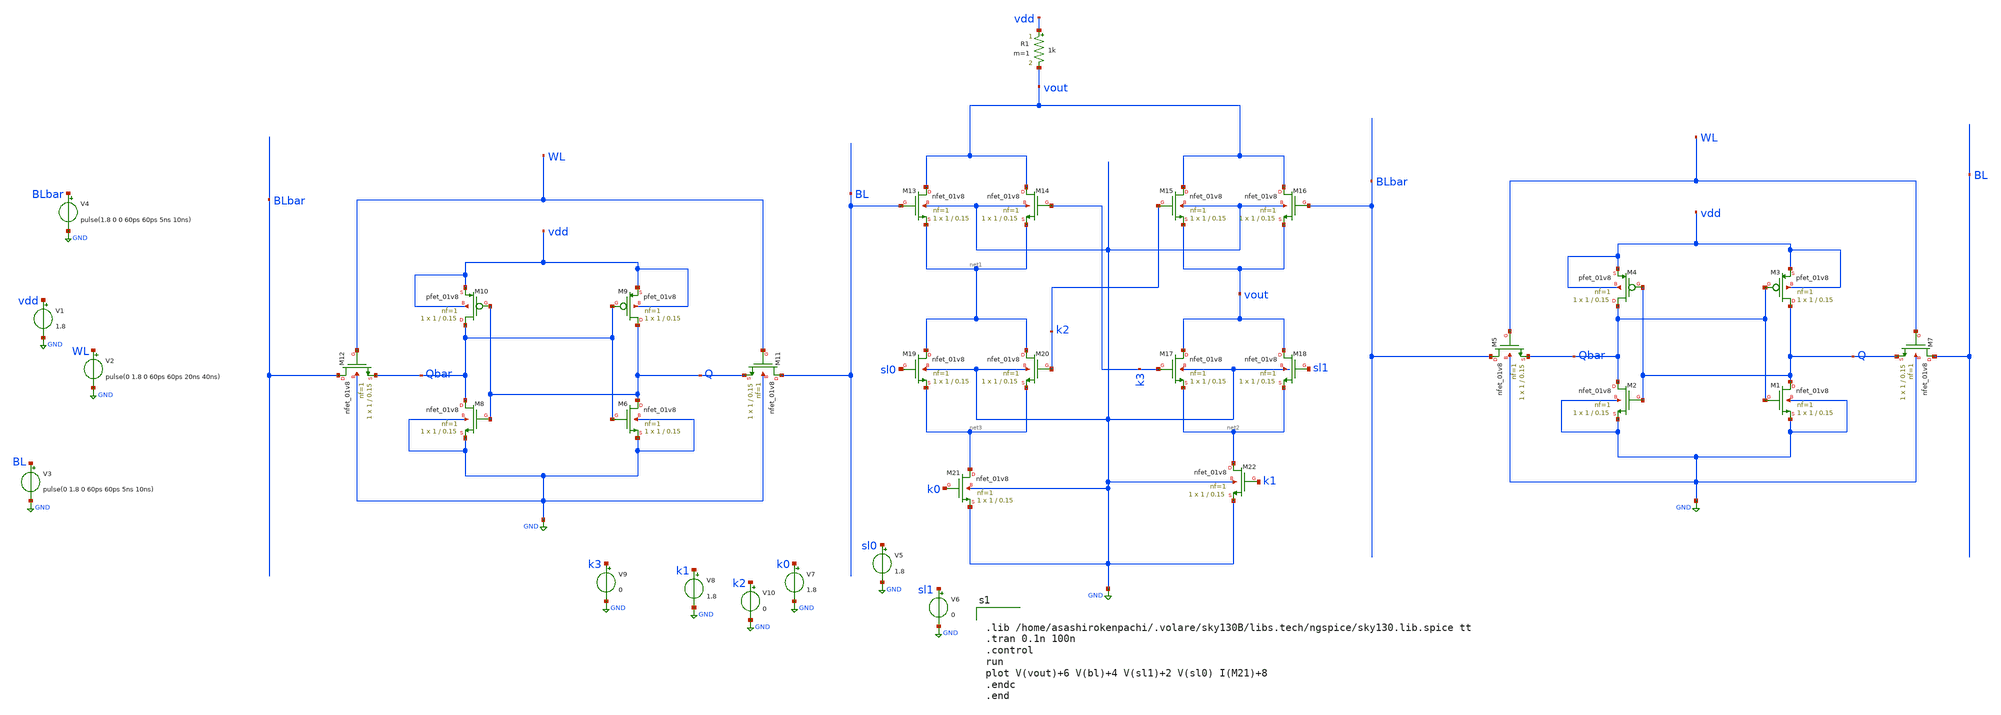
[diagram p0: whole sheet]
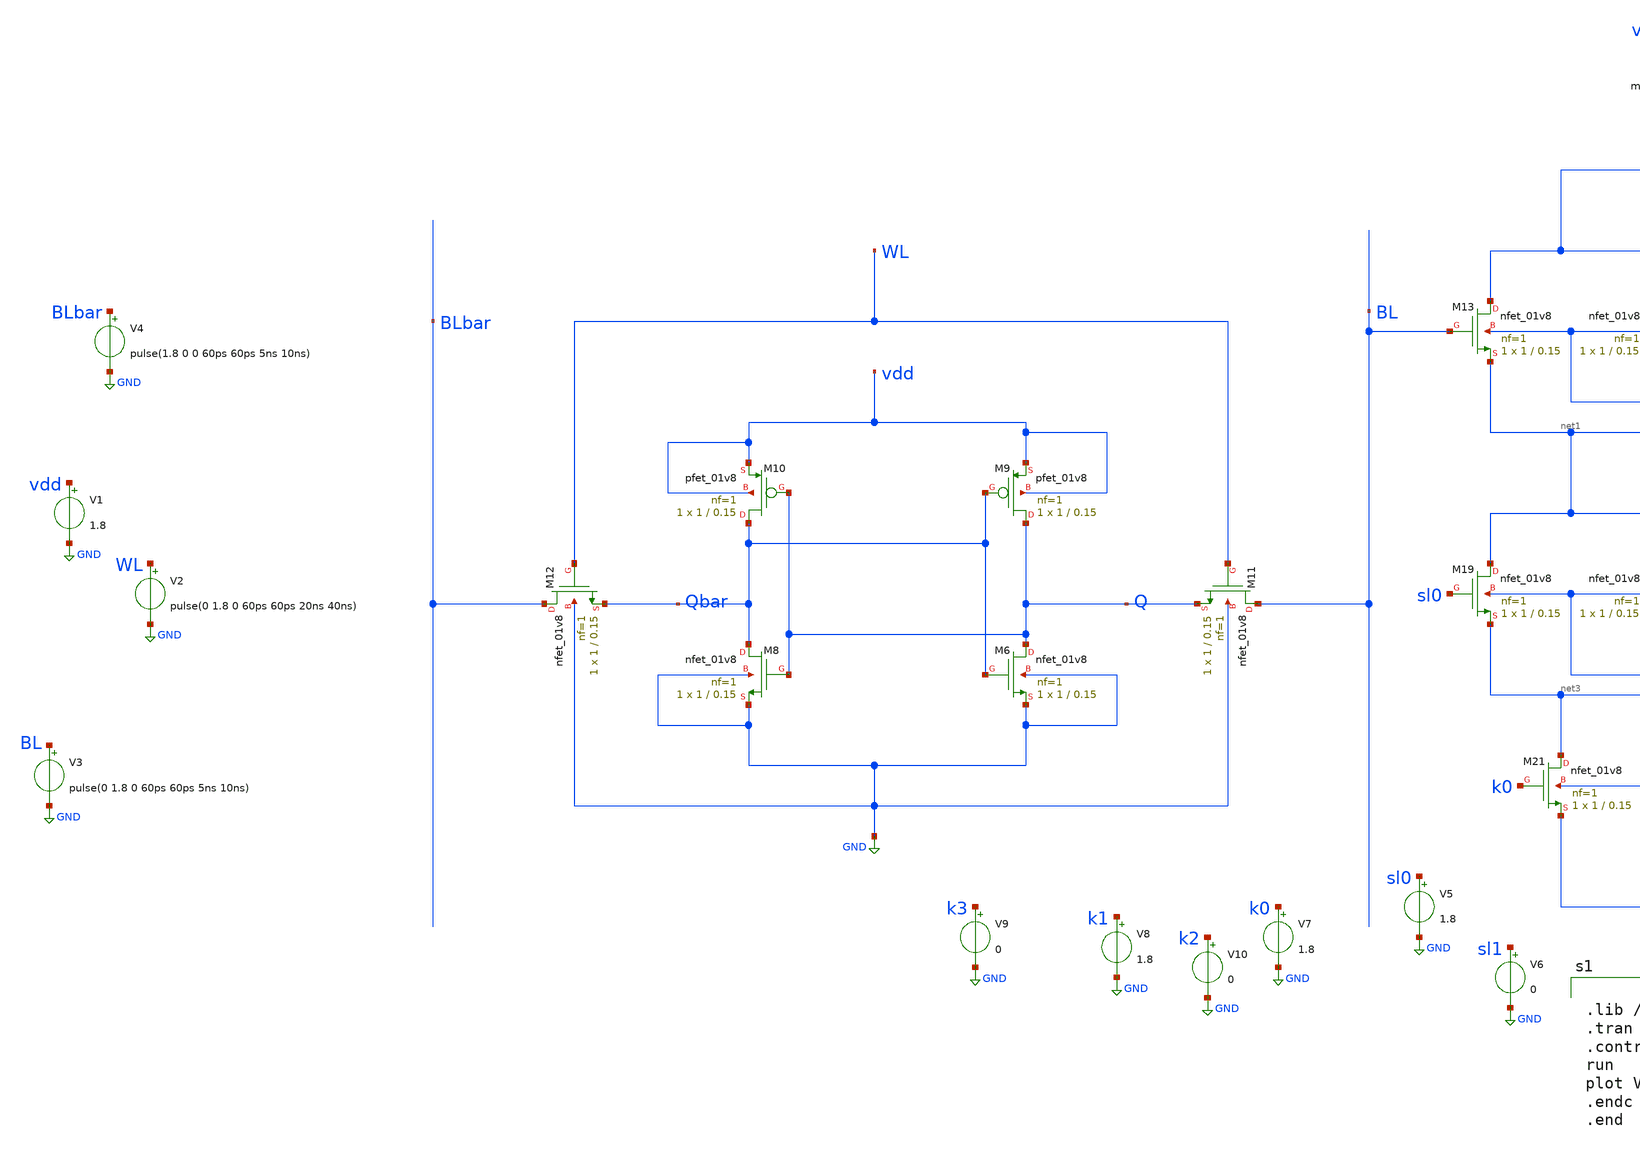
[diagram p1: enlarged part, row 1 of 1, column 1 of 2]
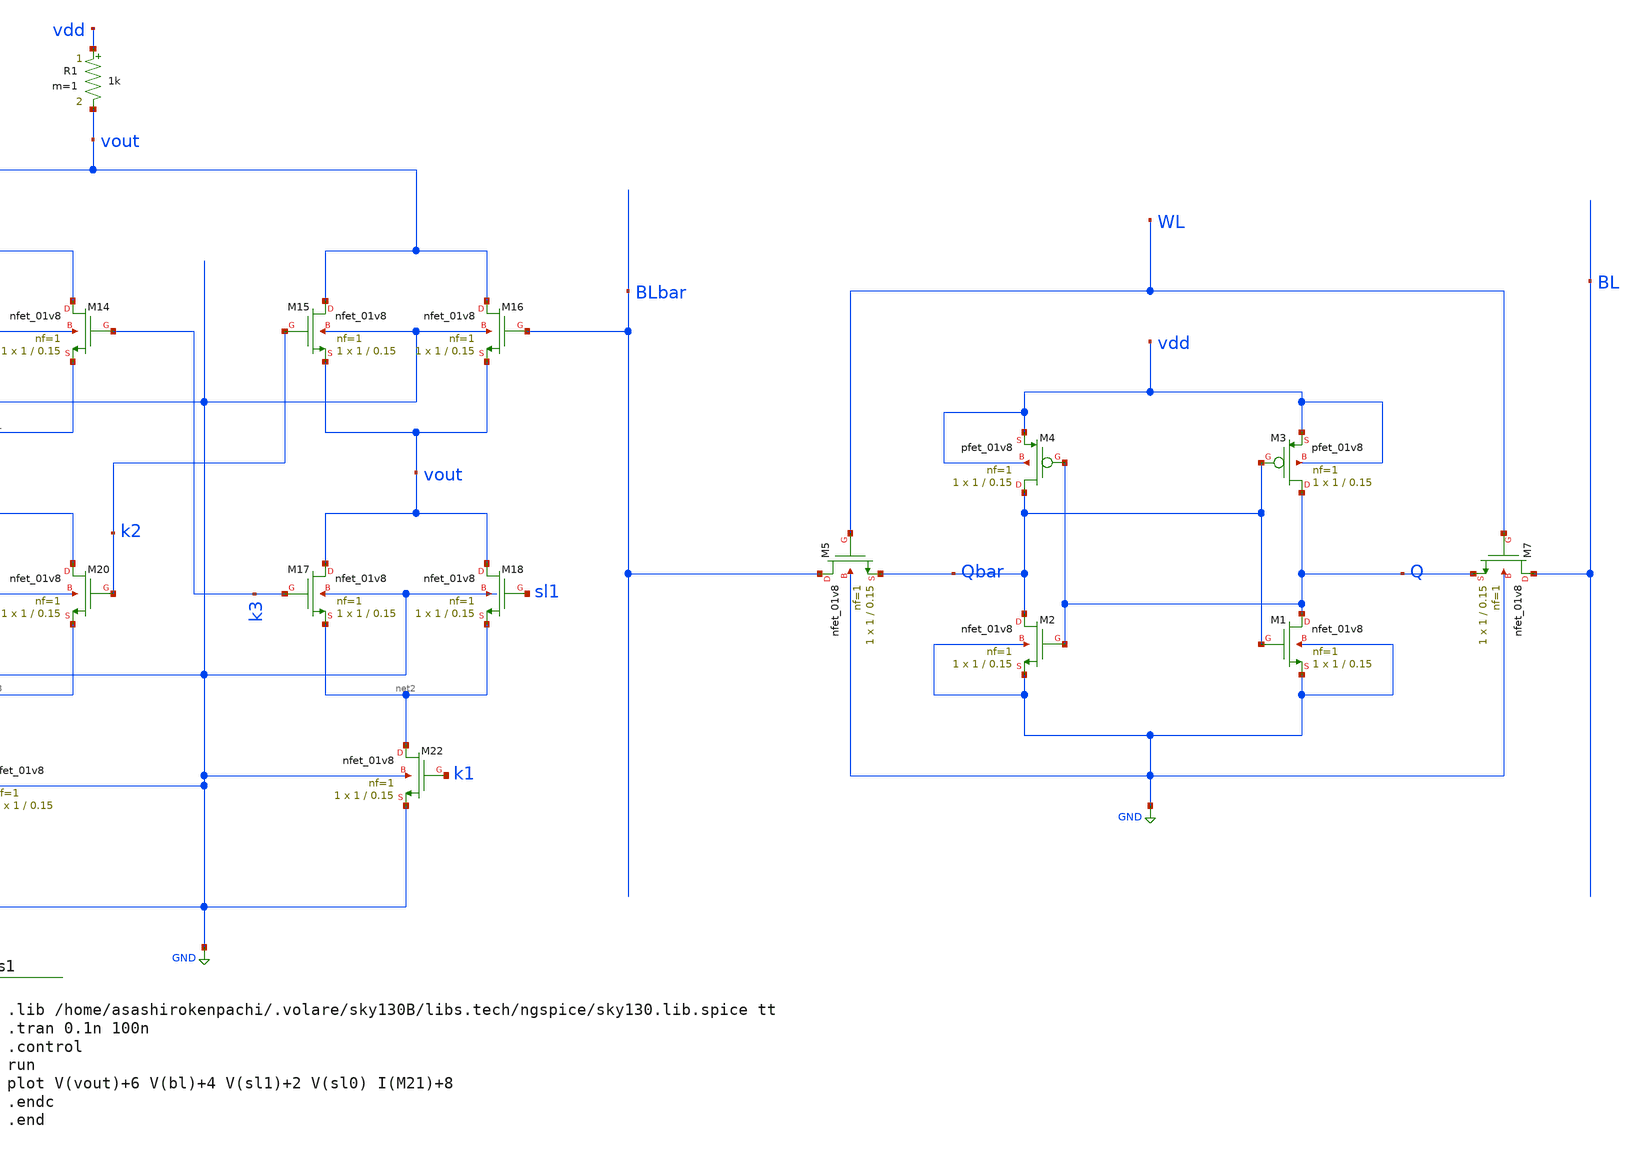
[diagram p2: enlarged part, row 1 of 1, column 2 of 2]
** sch_path: sram_cell_comp.sch
**.subckt sram_cell_comp
XM1 Q Qbar GND GND sky130_fd_pr__nfet_01v8 L=0.15 W=1 nf=1 ad='int((nf+1)/2) * W/nf * 0.29' as='int((nf+2)/2) * W/nf * 0.29'
+ pd='2*int((nf+1)/2) * (W/nf + 0.29)' ps='2*int((nf+2)/2) * (W/nf + 0.29)' nrd='0.29 / W' nrs='0.29 / W'
+ sa=0 sb=0 sd=0 mult=1 m=1
XM2 Qbar Q GND GND sky130_fd_pr__nfet_01v8 L=0.15 W=1 nf=1 ad='int((nf+1)/2) * W/nf * 0.29' as='int((nf+2)/2) * W/nf * 0.29'
+ pd='2*int((nf+1)/2) * (W/nf + 0.29)' ps='2*int((nf+2)/2) * (W/nf + 0.29)' nrd='0.29 / W' nrs='0.29 / W'
+ sa=0 sb=0 sd=0 mult=1 m=1
XM3 Q Qbar vdd vdd sky130_fd_pr__pfet_01v8 L=0.15 W=1 nf=1 ad='int((nf+1)/2) * W/nf * 0.29' as='int((nf+2)/2) * W/nf * 0.29'
+ pd='2*int((nf+1)/2) * (W/nf + 0.29)' ps='2*int((nf+2)/2) * (W/nf + 0.29)' nrd='0.29 / W' nrs='0.29 / W'
+ sa=0 sb=0 sd=0 mult=1 m=1
XM4 Qbar Q vdd vdd sky130_fd_pr__pfet_01v8 L=0.15 W=1 nf=1 ad='int((nf+1)/2) * W/nf * 0.29' as='int((nf+2)/2) * W/nf * 0.29'
+ pd='2*int((nf+1)/2) * (W/nf + 0.29)' ps='2*int((nf+2)/2) * (W/nf + 0.29)' nrd='0.29 / W' nrs='0.29 / W'
+ sa=0 sb=0 sd=0 mult=1 m=1
XM7 BL WL Q GND sky130_fd_pr__nfet_01v8 L=0.15 W=1 nf=1 ad='int((nf+1)/2) * W/nf * 0.29' as='int((nf+2)/2) * W/nf * 0.29'
+ pd='2*int((nf+1)/2) * (W/nf + 0.29)' ps='2*int((nf+2)/2) * (W/nf + 0.29)' nrd='0.29 / W' nrs='0.29 / W'
+ sa=0 sb=0 sd=0 mult=1 m=1
XM5 BLbar WL Qbar GND sky130_fd_pr__nfet_01v8 L=0.15 W=1 nf=1 ad='int((nf+1)/2) * W/nf * 0.29' as='int((nf+2)/2) * W/nf * 0.29'
+ pd='2*int((nf+1)/2) * (W/nf + 0.29)' ps='2*int((nf+2)/2) * (W/nf + 0.29)' nrd='0.29 / W' nrs='0.29 / W'
+ sa=0 sb=0 sd=0 mult=1 m=1
V1 vdd GND 1.8
V2 WL GND pulse(0 1.8 0 60ps 60ps 20ns 40ns)
V3 BL GND pulse(0 1.8 0 60ps 60ps 5ns 10ns)
V4 BLbar GND pulse(1.8 0 0 60ps 60ps 5ns 10ns)
XM6 Q Qbar GND GND sky130_fd_pr__nfet_01v8 L=0.15 W=1 nf=1 ad='int((nf+1)/2) * W/nf * 0.29' as='int((nf+2)/2) * W/nf * 0.29'
+ pd='2*int((nf+1)/2) * (W/nf + 0.29)' ps='2*int((nf+2)/2) * (W/nf + 0.29)' nrd='0.29 / W' nrs='0.29 / W'
+ sa=0 sb=0 sd=0 mult=1 m=1
XM8 Qbar Q GND GND sky130_fd_pr__nfet_01v8 L=0.15 W=1 nf=1 ad='int((nf+1)/2) * W/nf * 0.29' as='int((nf+2)/2) * W/nf * 0.29'
+ pd='2*int((nf+1)/2) * (W/nf + 0.29)' ps='2*int((nf+2)/2) * (W/nf + 0.29)' nrd='0.29 / W' nrs='0.29 / W'
+ sa=0 sb=0 sd=0 mult=1 m=1
XM9 Q Qbar vdd vdd sky130_fd_pr__pfet_01v8 L=0.15 W=1 nf=1 ad='int((nf+1)/2) * W/nf * 0.29' as='int((nf+2)/2) * W/nf * 0.29'
+ pd='2*int((nf+1)/2) * (W/nf + 0.29)' ps='2*int((nf+2)/2) * (W/nf + 0.29)' nrd='0.29 / W' nrs='0.29 / W'
+ sa=0 sb=0 sd=0 mult=1 m=1
XM10 Qbar Q vdd vdd sky130_fd_pr__pfet_01v8 L=0.15 W=1 nf=1 ad='int((nf+1)/2) * W/nf * 0.29' as='int((nf+2)/2) * W/nf * 0.29'
+ pd='2*int((nf+1)/2) * (W/nf + 0.29)' ps='2*int((nf+2)/2) * (W/nf + 0.29)' nrd='0.29 / W' nrs='0.29 / W'
+ sa=0 sb=0 sd=0 mult=1 m=1
XM11 BL WL Q GND sky130_fd_pr__nfet_01v8 L=0.15 W=1 nf=1 ad='int((nf+1)/2) * W/nf * 0.29' as='int((nf+2)/2) * W/nf * 0.29'
+ pd='2*int((nf+1)/2) * (W/nf + 0.29)' ps='2*int((nf+2)/2) * (W/nf + 0.29)' nrd='0.29 / W' nrs='0.29 / W'
+ sa=0 sb=0 sd=0 mult=1 m=1
XM12 BLbar WL Qbar GND sky130_fd_pr__nfet_01v8 L=0.15 W=1 nf=1 ad='int((nf+1)/2) * W/nf * 0.29' as='int((nf+2)/2) * W/nf * 0.29'
+ pd='2*int((nf+1)/2) * (W/nf + 0.29)' ps='2*int((nf+2)/2) * (W/nf + 0.29)' nrd='0.29 / W' nrs='0.29 / W'
+ sa=0 sb=0 sd=0 mult=1 m=1
XM13 vout BL net1 GND sky130_fd_pr__nfet_01v8 L=0.15 W=1 nf=1 ad='int((nf+1)/2) * W/nf * 0.29' as='int((nf+2)/2) * W/nf * 0.29'
+ pd='2*int((nf+1)/2) * (W/nf + 0.29)' ps='2*int((nf+2)/2) * (W/nf + 0.29)' nrd='0.29 / W' nrs='0.29 / W'
+ sa=0 sb=0 sd=0 mult=1 m=1
XM14 vout k3 net1 GND sky130_fd_pr__nfet_01v8 L=0.15 W=1 nf=1 ad='int((nf+1)/2) * W/nf * 0.29' as='int((nf+2)/2) * W/nf * 0.29'
+ pd='2*int((nf+1)/2) * (W/nf + 0.29)' ps='2*int((nf+2)/2) * (W/nf + 0.29)' nrd='0.29 / W' nrs='0.29 / W'
+ sa=0 sb=0 sd=0 mult=1 m=1
XM15 vout k2 vout GND sky130_fd_pr__nfet_01v8 L=0.15 W=1 nf=1 ad='int((nf+1)/2) * W/nf * 0.29' as='int((nf+2)/2) * W/nf * 0.29'
+ pd='2*int((nf+1)/2) * (W/nf + 0.29)' ps='2*int((nf+2)/2) * (W/nf + 0.29)' nrd='0.29 / W' nrs='0.29 / W'
+ sa=0 sb=0 sd=0 mult=1 m=1
XM16 vout BLbar vout GND sky130_fd_pr__nfet_01v8 L=0.15 W=1 nf=1 ad='int((nf+1)/2) * W/nf * 0.29' as='int((nf+2)/2) * W/nf * 0.29'
+ pd='2*int((nf+1)/2) * (W/nf + 0.29)' ps='2*int((nf+2)/2) * (W/nf + 0.29)' nrd='0.29 / W' nrs='0.29 / W'
+ sa=0 sb=0 sd=0 mult=1 m=1
XM17 vout k3 net2 GND sky130_fd_pr__nfet_01v8 L=0.15 W=1 nf=1 ad='int((nf+1)/2) * W/nf * 0.29' as='int((nf+2)/2) * W/nf * 0.29'
+ pd='2*int((nf+1)/2) * (W/nf + 0.29)' ps='2*int((nf+2)/2) * (W/nf + 0.29)' nrd='0.29 / W' nrs='0.29 / W'
+ sa=0 sb=0 sd=0 mult=1 m=1
XM18 vout sl1 net2 GND sky130_fd_pr__nfet_01v8 L=0.15 W=1 nf=1 ad='int((nf+1)/2) * W/nf * 0.29' as='int((nf+2)/2) * W/nf * 0.29'
+ pd='2*int((nf+1)/2) * (W/nf + 0.29)' ps='2*int((nf+2)/2) * (W/nf + 0.29)' nrd='0.29 / W' nrs='0.29 / W'
+ sa=0 sb=0 sd=0 mult=1 m=1
XM19 net1 sl0 net3 GND sky130_fd_pr__nfet_01v8 L=0.15 W=1 nf=1 ad='int((nf+1)/2) * W/nf * 0.29' as='int((nf+2)/2) * W/nf * 0.29'
+ pd='2*int((nf+1)/2) * (W/nf + 0.29)' ps='2*int((nf+2)/2) * (W/nf + 0.29)' nrd='0.29 / W' nrs='0.29 / W'
+ sa=0 sb=0 sd=0 mult=1 m=1
XM20 net1 k2 net3 GND sky130_fd_pr__nfet_01v8 L=0.15 W=1 nf=1 ad='int((nf+1)/2) * W/nf * 0.29' as='int((nf+2)/2) * W/nf * 0.29'
+ pd='2*int((nf+1)/2) * (W/nf + 0.29)' ps='2*int((nf+2)/2) * (W/nf + 0.29)' nrd='0.29 / W' nrs='0.29 / W'
+ sa=0 sb=0 sd=0 mult=1 m=1
XM21 net3 k0 GND GND sky130_fd_pr__nfet_01v8 L=0.15 W=1 nf=1 ad='int((nf+1)/2) * W/nf * 0.29' as='int((nf+2)/2) * W/nf * 0.29'
+ pd='2*int((nf+1)/2) * (W/nf + 0.29)' ps='2*int((nf+2)/2) * (W/nf + 0.29)' nrd='0.29 / W' nrs='0.29 / W'
+ sa=0 sb=0 sd=0 mult=1 m=1
XM22 net2 k1 GND GND sky130_fd_pr__nfet_01v8 L=0.15 W=1 nf=1 ad='int((nf+1)/2) * W/nf * 0.29' as='int((nf+2)/2) * W/nf * 0.29'
+ pd='2*int((nf+1)/2) * (W/nf + 0.29)' ps='2*int((nf+2)/2) * (W/nf + 0.29)' nrd='0.29 / W' nrs='0.29 / W'
+ sa=0 sb=0 sd=0 mult=1 m=1
V5 sl0 GND 1.8
V6 sl1 GND 0
V7 k0 GND 1.8
V8 k1 GND 1.8
V9 k3 GND 0
V10 k2 GND 0
R1 vdd vout 1k m=1
**** begin user architecture code


.lib /home/asashirokenpachi/.volare/sky130B/libs.tech/ngspice/sky130.lib.spice tt
.tran 0.1n 100n
.control
run
plot V(vout)+6 V(bl)+4 V(sl1)+2 V(sl0) I(M21)+8
.endc
.end

**** end user architecture code
**.ends
.GLOBAL GND
.end
